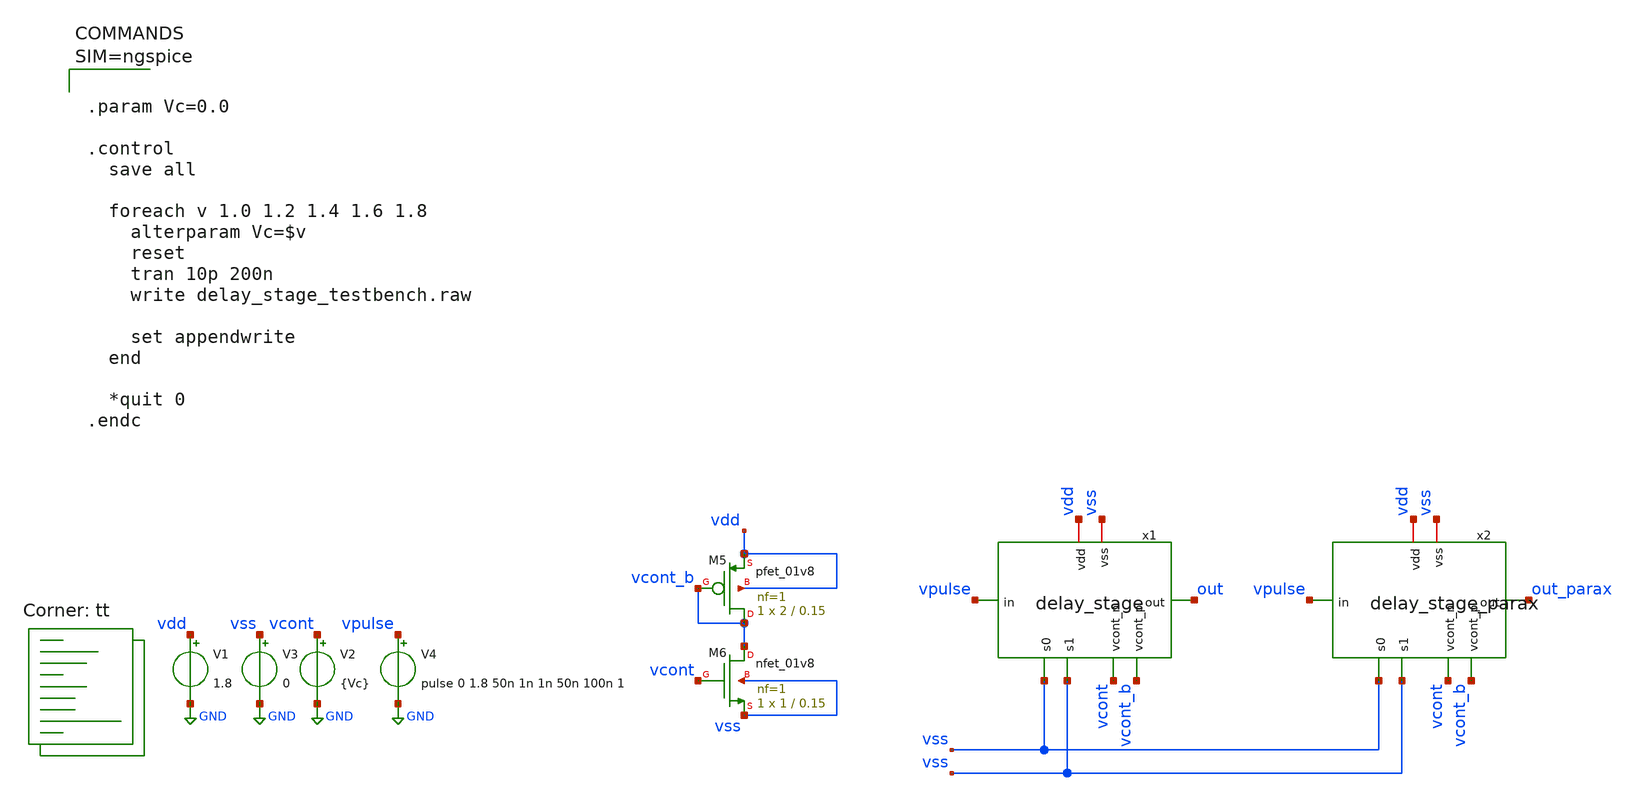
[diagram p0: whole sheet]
** sch_path: xschem/delay_stage_testbench.sch
**.subckt delay_stage_testbench
V1 vdd GND 1.8
V2 vcont GND {Vc}
V3 vss GND 0
x1 vdd vcont_b vss vss out vpulse vcont vss delay_stage
XM5 vcont_b vcont_b vdd vdd sky130_fd_pr__pfet_01v8 L=0.15 W=2 nf=1 ad='int((nf+1)/2) * W/nf * 0.29'
+ as='int((nf+2)/2) * W/nf * 0.29' pd='2*int((nf+1)/2) * (W/nf + 0.29)' ps='2*int((nf+2)/2) * (W/nf + 0.29)'
+ nrd='0.29 / W' nrs='0.29 / W' sa=0 sb=0 sd=0 mult=1 m=1
XM6 vcont_b vcont vss vss sky130_fd_pr__nfet_01v8 L=0.15 W=1 nf=1 ad='int((nf+1)/2) * W/nf * 0.29' as='int((nf+2)/2) * W/nf * 0.29'
+ pd='2*int((nf+1)/2) * (W/nf + 0.29)' ps='2*int((nf+2)/2) * (W/nf + 0.29)' nrd='0.29 / W' nrs='0.29 / W'
+ sa=0 sb=0 sd=0 mult=1 m=1
V4 vpulse GND pulse 0 1.8 50n 1n 1n 50n 100n 1
x2 vdd vcont_b vss vss out_parax vpulse vcont vss delay_stage_parax
**** begin user architecture code
.lib $::SKYWATER_MODELS/sky130.lib.spice tt



.param Vc=0.0

.control
  save all

  foreach v 1.0 1.2 1.4 1.6 1.8
    alterparam Vc=$v
    reset
    tran 10p 200n
    write delay_stage_testbench.raw

    set appendwrite
  end

  *quit 0
.endc



**** end user architecture code
**.ends

* expanding   symbol:  delay_stage.sym # of pins=8
** sym_path: xschem/delay_stage.sym
** sch_path: xschem/delay_stage.sch
.subckt delay_stage vdd vcont_p s0 s1 out in vcont_n vss
*.ipin in
*.opin out
*.iopin vdd
*.ipin vcont_n
*.ipin vcont_p
*.ipin s0
*.ipin s1
*.iopin vss
XM3 out in net2 vss sky130_fd_pr__nfet_01v8 L=0.15 W=1 nf=1 ad='int((nf+1)/2) * W/nf * 0.29' as='int((nf+2)/2) * W/nf * 0.29'
+ pd='2*int((nf+1)/2) * (W/nf + 0.29)' ps='2*int((nf+2)/2) * (W/nf + 0.29)' nrd='0.29 / W' nrs='0.29 / W'
+ sa=0 sb=0 sd=0 mult=1 m=1
XM2 out in net1 vdd sky130_fd_pr__pfet_01v8 L=0.15 W=2 nf=1 ad='int((nf+1)/2) * W/nf * 0.29' as='int((nf+2)/2) * W/nf * 0.29'
+ pd='2*int((nf+1)/2) * (W/nf + 0.29)' ps='2*int((nf+2)/2) * (W/nf + 0.29)' nrd='0.29 / W' nrs='0.29 / W'
+ sa=0 sb=0 sd=0 mult=1 m=1
XM1 net1 vcont_p vdd vdd sky130_fd_pr__pfet_01v8 L=0.15 W=2 nf=1 ad='int((nf+1)/2) * W/nf * 0.29' as='int((nf+2)/2) * W/nf * 0.29'
+ pd='2*int((nf+1)/2) * (W/nf + 0.29)' ps='2*int((nf+2)/2) * (W/nf + 0.29)' nrd='0.29 / W' nrs='0.29 / W'
+ sa=0 sb=0 sd=0 mult=1 m=1
XM4 net2 vcont_n vss vss sky130_fd_pr__nfet_01v8 L=0.15 W=1 nf=1 ad='int((nf+1)/2) * W/nf * 0.29' as='int((nf+2)/2) * W/nf * 0.29'
+ pd='2*int((nf+1)/2) * (W/nf + 0.29)' ps='2*int((nf+2)/2) * (W/nf + 0.29)' nrd='0.29 / W' nrs='0.29 / W'
+ sa=0 sb=0 sd=0 mult=1 m=1
XC2 net3 vss sky130_fd_pr__cap_mim_m3_1 W=2.1 L=2.1 MF=1 m=1
XC1 net4 vss sky130_fd_pr__cap_mim_m3_1 W=2.1 L=4.2 MF=1 m=1
XM5 out s0 net4 vss sky130_fd_pr__nfet_01v8 L=0.15 W=1 nf=1 ad='int((nf+1)/2) * W/nf * 0.29' as='int((nf+2)/2) * W/nf * 0.29'
+ pd='2*int((nf+1)/2) * (W/nf + 0.29)' ps='2*int((nf+2)/2) * (W/nf + 0.29)' nrd='0.29 / W' nrs='0.29 / W'
+ sa=0 sb=0 sd=0 mult=1 m=1
XM6 out s1 net3 vss sky130_fd_pr__nfet_01v8 L=0.15 W=1 nf=1 ad='int((nf+1)/2) * W/nf * 0.29' as='int((nf+2)/2) * W/nf * 0.29'
+ pd='2*int((nf+1)/2) * (W/nf + 0.29)' ps='2*int((nf+2)/2) * (W/nf + 0.29)' nrd='0.29 / W' nrs='0.29 / W'
+ sa=0 sb=0 sd=0 mult=1 m=1
.ends


* expanding   symbol:  delay_stage_parax.sym # of pins=8
** sym_path: xschem/delay_stage.sym
.include [file normalize ../mag/delay_stage.sim.spice]
.GLOBAL GND
.end
